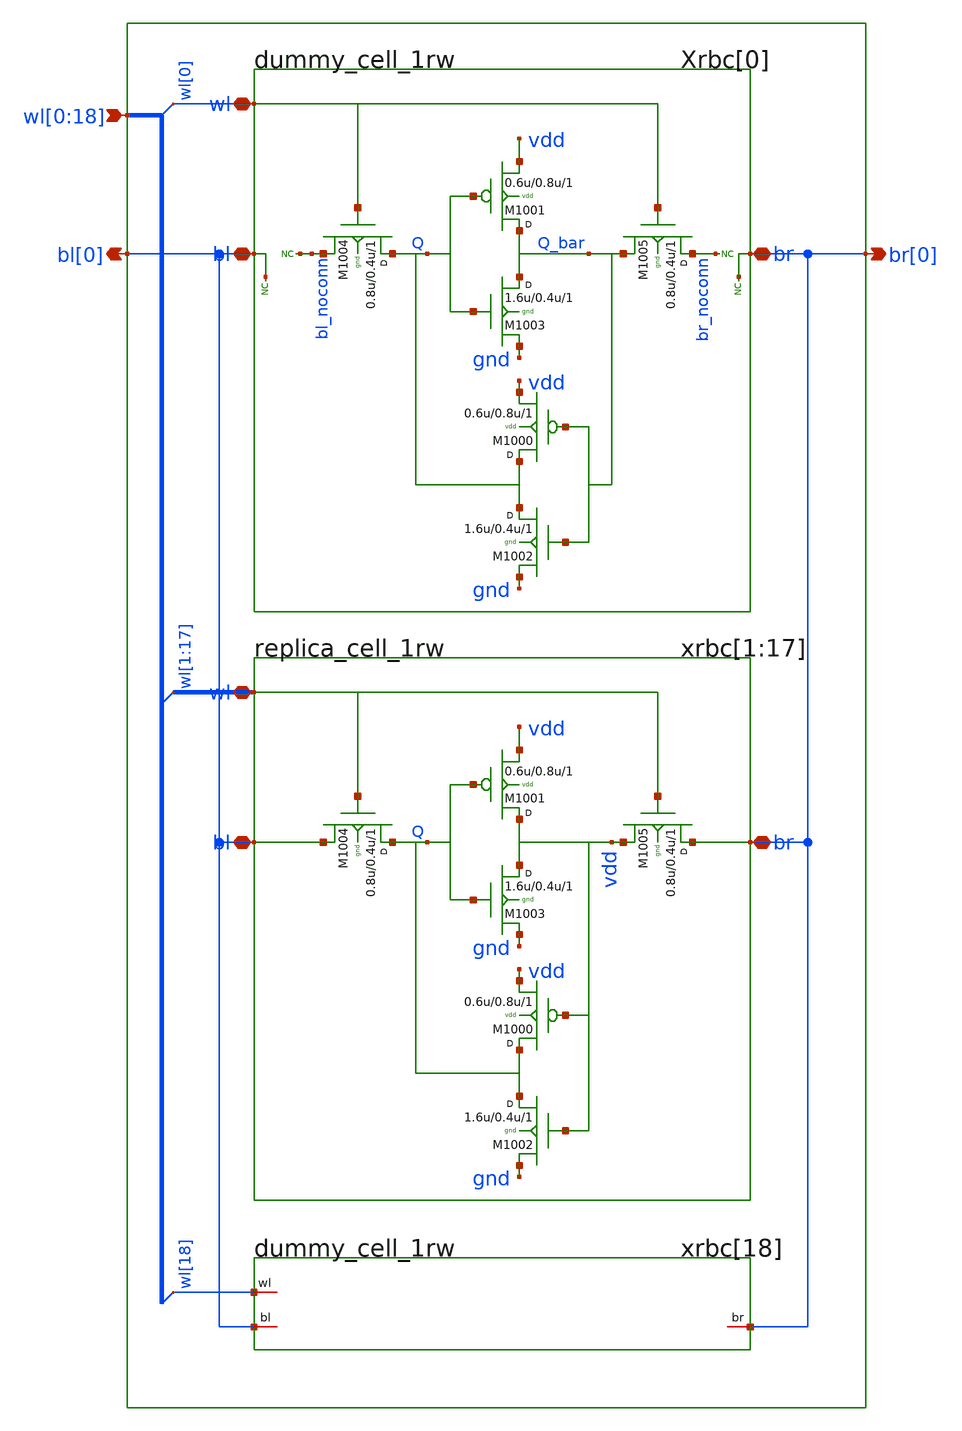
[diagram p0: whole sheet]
** sch_path: sram_2_64_scn4m/replica_column.sch
**.subckt replica_column bl[0] br[0]
*+ wl[0],wl[1],wl[2],wl[3],wl[4],wl[5],wl[6],wl[7],wl[8],wl[9],wl[10],wl[11],wl[12],wl[13],wl[14],wl[15],wl[16],wl[17],wl[18]
*.opin bl[0]
*.opin br[0]
*.ipin
*+ wl[0],wl[1],wl[2],wl[3],wl[4],wl[5],wl[6],wl[7],wl[8],wl[9],wl[10],wl[11],wl[12],wl[13],wl[14],wl[15],wl[16],wl[17],wl[18]
Xrbc[0] bl[0] br[0] wl[0] vdd gnd dummy_cell_1rw
xrbc[1] bl[0] br[0] wl[1] vdd gnd replica_cell_1rw
xrbc[2] bl[0] br[0] wl[2] vdd gnd replica_cell_1rw
xrbc[3] bl[0] br[0] wl[3] vdd gnd replica_cell_1rw
xrbc[4] bl[0] br[0] wl[4] vdd gnd replica_cell_1rw
xrbc[5] bl[0] br[0] wl[5] vdd gnd replica_cell_1rw
xrbc[6] bl[0] br[0] wl[6] vdd gnd replica_cell_1rw
xrbc[7] bl[0] br[0] wl[7] vdd gnd replica_cell_1rw
xrbc[8] bl[0] br[0] wl[8] vdd gnd replica_cell_1rw
xrbc[9] bl[0] br[0] wl[9] vdd gnd replica_cell_1rw
xrbc[10] bl[0] br[0] wl[10] vdd gnd replica_cell_1rw
xrbc[11] bl[0] br[0] wl[11] vdd gnd replica_cell_1rw
xrbc[12] bl[0] br[0] wl[12] vdd gnd replica_cell_1rw
xrbc[13] bl[0] br[0] wl[13] vdd gnd replica_cell_1rw
xrbc[14] bl[0] br[0] wl[14] vdd gnd replica_cell_1rw
xrbc[15] bl[0] br[0] wl[15] vdd gnd replica_cell_1rw
xrbc[16] bl[0] br[0] wl[16] vdd gnd replica_cell_1rw
xrbc[17] bl[0] br[0] wl[17] vdd gnd replica_cell_1rw
xrbc[18] bl[0] br[0] wl[18] vdd gnd dummy_cell_1rw
**.ends
.end
